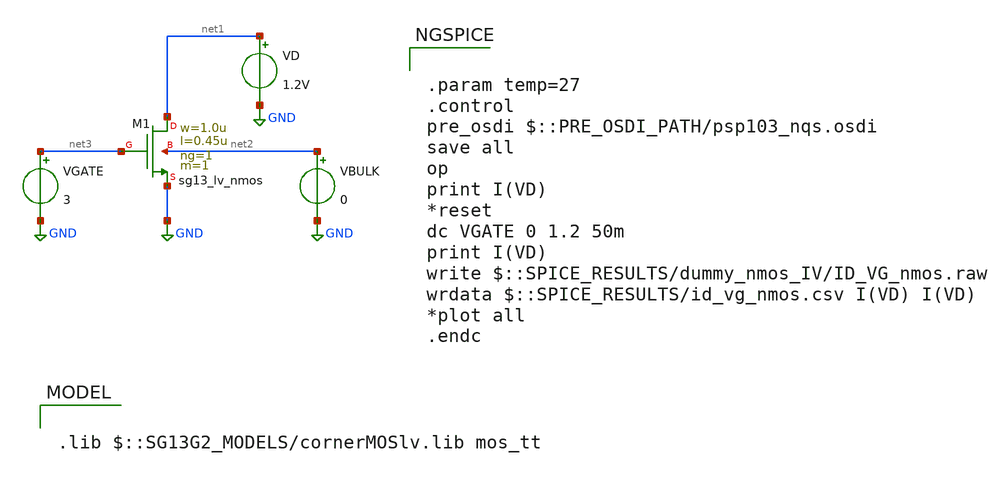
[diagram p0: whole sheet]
** sch_path: exp/IHP130/dummy_nmos_IV/nmos_ID_vs_VG.sch
**.subckt nmos_ID_vs_VG
XM1 net1 net3 GND net2 sg13_lv_nmos w=1.0u l=0.45u ng=1 m=1 mm_ok=1
VD net1 GND 1.2V
VGATE net3 GND 3
VBULK net2 GND 0
**** begin user architecture code

.param temp=27
.control
pre_osdi $::PRE_OSDI_PATH/psp103_nqs.osdi
save all
op
print I(VD)
*reset
dc VGATE 0 1.2 50m
print I(VD)
write $::SPICE_RESULTS/dummy_nmos_IV/ID_VG_nmos.raw
wrdata $::SPICE_RESULTS/id_vg_nmos.csv I(VD) I(VD)
*plot all
.endc


.lib $::SG13G2_MODELS/cornerMOSlv.lib mos_tt

**** end user architecture code
**.ends
.GLOBAL GND
.end
